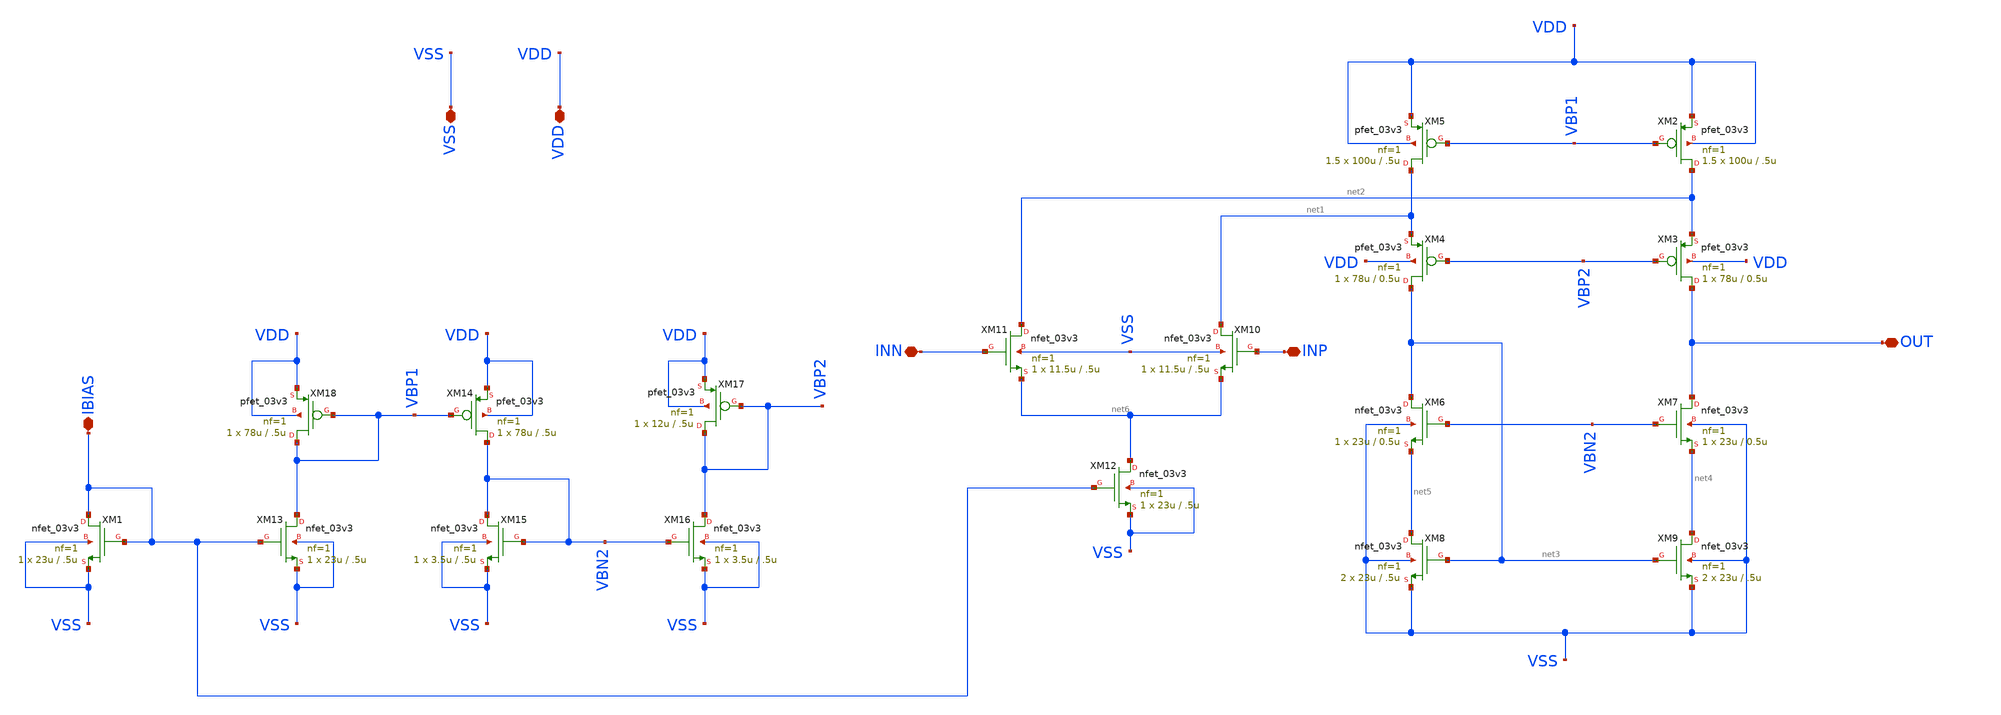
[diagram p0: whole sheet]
** sch_path: designs/libs/core_amps/ota_folded_cascode/ota_folded_cascode.sch
**.subckt ota_folded_cascode IBIAS VSS VDD INN INP OUT
*.iopin IBIAS
*.iopin VSS
*.iopin VDD
*.iopin INN
*.iopin INP
*.iopin OUT
XM1 IBIAS IBIAS VSS VSS nfet_03v3 L=.5u W=23u nf=1 ad='int((nf+1)/2) * W/nf * 0.18u' as='int((nf+2)/2) * W/nf * 0.18u'
+ pd='2*int((nf+1)/2) * (W/nf + 0.18u)' ps='2*int((nf+2)/2) * (W/nf + 0.18u)' nrd='0.18u / W' nrs='0.18u / W'
+ sa=0 sb=0 sd=0 m=1
XM2 net2 VBP1 VDD VDD pfet_03v3 L=.5u W=100u nf=1 ad='int((nf+1)/2) * W/nf * 0.18u' as='int((nf+2)/2) * W/nf * 0.18u'
+ pd='2*int((nf+1)/2) * (W/nf + 0.18u)' ps='2*int((nf+2)/2) * (W/nf + 0.18u)' nrd='0.18u / W' nrs='0.18u / W'
+ sa=0 sb=0 sd=0 m=1.5
XM3 OUT VBP2 net2 VDD pfet_03v3 L=0.5u W=78u nf=1 ad='int((nf+1)/2) * W/nf * 0.18u' as='int((nf+2)/2) * W/nf * 0.18u'
+ pd='2*int((nf+1)/2) * (W/nf + 0.18u)' ps='2*int((nf+2)/2) * (W/nf + 0.18u)' nrd='0.18u / W' nrs='0.18u / W'
+ sa=0 sb=0 sd=0 m=1
XM4 net3 VBP2 net1 VDD pfet_03v3 L=0.5u W=78u nf=1 ad='int((nf+1)/2) * W/nf * 0.18u' as='int((nf+2)/2) * W/nf * 0.18u'
+ pd='2*int((nf+1)/2) * (W/nf + 0.18u)' ps='2*int((nf+2)/2) * (W/nf + 0.18u)' nrd='0.18u / W' nrs='0.18u / W'
+ sa=0 sb=0 sd=0 m=1
XM5 net1 VBP1 VDD VDD pfet_03v3 L=.5u W=100u nf=1 ad='int((nf+1)/2) * W/nf * 0.18u' as='int((nf+2)/2) * W/nf * 0.18u'
+ pd='2*int((nf+1)/2) * (W/nf + 0.18u)' ps='2*int((nf+2)/2) * (W/nf + 0.18u)' nrd='0.18u / W' nrs='0.18u / W'
+ sa=0 sb=0 sd=0 m=1.5
XM6 net3 VBN2 net5 VSS nfet_03v3 L=0.5u W=23u nf=1 ad='int((nf+1)/2) * W/nf * 0.18u' as='int((nf+2)/2) * W/nf * 0.18u'
+ pd='2*int((nf+1)/2) * (W/nf + 0.18u)' ps='2*int((nf+2)/2) * (W/nf + 0.18u)' nrd='0.18u / W' nrs='0.18u / W'
+ sa=0 sb=0 sd=0 m=1
XM7 OUT VBN2 net4 VSS nfet_03v3 L=0.5u W=23u nf=1 ad='int((nf+1)/2) * W/nf * 0.18u' as='int((nf+2)/2) * W/nf * 0.18u'
+ pd='2*int((nf+1)/2) * (W/nf + 0.18u)' ps='2*int((nf+2)/2) * (W/nf + 0.18u)' nrd='0.18u / W' nrs='0.18u / W'
+ sa=0 sb=0 sd=0 m=1
XM8 net5 net3 VSS VSS nfet_03v3 L=.5u W=23u nf=1 ad='int((nf+1)/2) * W/nf * 0.18u' as='int((nf+2)/2) * W/nf * 0.18u'
+ pd='2*int((nf+1)/2) * (W/nf + 0.18u)' ps='2*int((nf+2)/2) * (W/nf + 0.18u)' nrd='0.18u / W' nrs='0.18u / W'
+ sa=0 sb=0 sd=0 m=2
XM9 net4 net3 VSS VSS nfet_03v3 L=.5u W=23u nf=1 ad='int((nf+1)/2) * W/nf * 0.18u' as='int((nf+2)/2) * W/nf * 0.18u'
+ pd='2*int((nf+1)/2) * (W/nf + 0.18u)' ps='2*int((nf+2)/2) * (W/nf + 0.18u)' nrd='0.18u / W' nrs='0.18u / W'
+ sa=0 sb=0 sd=0 m=2
XM10 net1 INP net6 VSS nfet_03v3 L=.5u W=11.5u nf=1 ad='int((nf+1)/2) * W/nf * 0.18u' as='int((nf+2)/2) * W/nf * 0.18u'
+ pd='2*int((nf+1)/2) * (W/nf + 0.18u)' ps='2*int((nf+2)/2) * (W/nf + 0.18u)' nrd='0.18u / W' nrs='0.18u / W'
+ sa=0 sb=0 sd=0 m=1
XM12 net6 IBIAS VSS VSS nfet_03v3 L=.5u W=23u nf=1 ad='int((nf+1)/2) * W/nf * 0.18u' as='int((nf+2)/2) * W/nf * 0.18u'
+ pd='2*int((nf+1)/2) * (W/nf + 0.18u)' ps='2*int((nf+2)/2) * (W/nf + 0.18u)' nrd='0.18u / W' nrs='0.18u / W'
+ sa=0 sb=0 sd=0 m=1
XM18 VBP1 VBP1 VDD VDD pfet_03v3 L=.5u W=78u nf=1 ad='int((nf+1)/2) * W/nf * 0.18u' as='int((nf+2)/2) * W/nf * 0.18u'
+ pd='2*int((nf+1)/2) * (W/nf + 0.18u)' ps='2*int((nf+2)/2) * (W/nf + 0.18u)' nrd='0.18u / W' nrs='0.18u / W'
+ sa=0 sb=0 sd=0 m=1
XM11 net2 INN net6 VSS nfet_03v3 L=.5u W=11.5u nf=1 ad='int((nf+1)/2) * W/nf * 0.18u' as='int((nf+2)/2) * W/nf * 0.18u'
+ pd='2*int((nf+1)/2) * (W/nf + 0.18u)' ps='2*int((nf+2)/2) * (W/nf + 0.18u)' nrd='0.18u / W' nrs='0.18u / W'
+ sa=0 sb=0 sd=0 m=1
XM13 VBP1 IBIAS VSS VSS nfet_03v3 L=.5u W=23u nf=1 ad='int((nf+1)/2) * W/nf * 0.18u' as='int((nf+2)/2) * W/nf * 0.18u'
+ pd='2*int((nf+1)/2) * (W/nf + 0.18u)' ps='2*int((nf+2)/2) * (W/nf + 0.18u)' nrd='0.18u / W' nrs='0.18u / W'
+ sa=0 sb=0 sd=0 m=1
XM14 VBN2 VBP1 VDD VDD pfet_03v3 L=.5u W=78u nf=1 ad='int((nf+1)/2) * W/nf * 0.18u' as='int((nf+2)/2) * W/nf * 0.18u'
+ pd='2*int((nf+1)/2) * (W/nf + 0.18u)' ps='2*int((nf+2)/2) * (W/nf + 0.18u)' nrd='0.18u / W' nrs='0.18u / W'
+ sa=0 sb=0 sd=0 m=1
XM15 VBN2 VBN2 VSS VSS nfet_03v3 L=.5u W=3.5u nf=1 ad='int((nf+1)/2) * W/nf * 0.18u' as='int((nf+2)/2) * W/nf * 0.18u'
+ pd='2*int((nf+1)/2) * (W/nf + 0.18u)' ps='2*int((nf+2)/2) * (W/nf + 0.18u)' nrd='0.18u / W' nrs='0.18u / W'
+ sa=0 sb=0 sd=0 m=1
XM16 VBP2 VBN2 VSS VSS nfet_03v3 L=.5u W=3.5u nf=1 ad='int((nf+1)/2) * W/nf * 0.18u' as='int((nf+2)/2) * W/nf * 0.18u'
+ pd='2*int((nf+1)/2) * (W/nf + 0.18u)' ps='2*int((nf+2)/2) * (W/nf + 0.18u)' nrd='0.18u / W' nrs='0.18u / W'
+ sa=0 sb=0 sd=0 m=1
XM17 VBP2 VBP2 VDD VDD pfet_03v3 L=.5u W=12u nf=1 ad='int((nf+1)/2) * W/nf * 0.18u' as='int((nf+2)/2) * W/nf * 0.18u'
+ pd='2*int((nf+1)/2) * (W/nf + 0.18u)' ps='2*int((nf+2)/2) * (W/nf + 0.18u)' nrd='0.18u / W' nrs='0.18u / W'
+ sa=0 sb=0 sd=0 m=1
**.ends
.end
